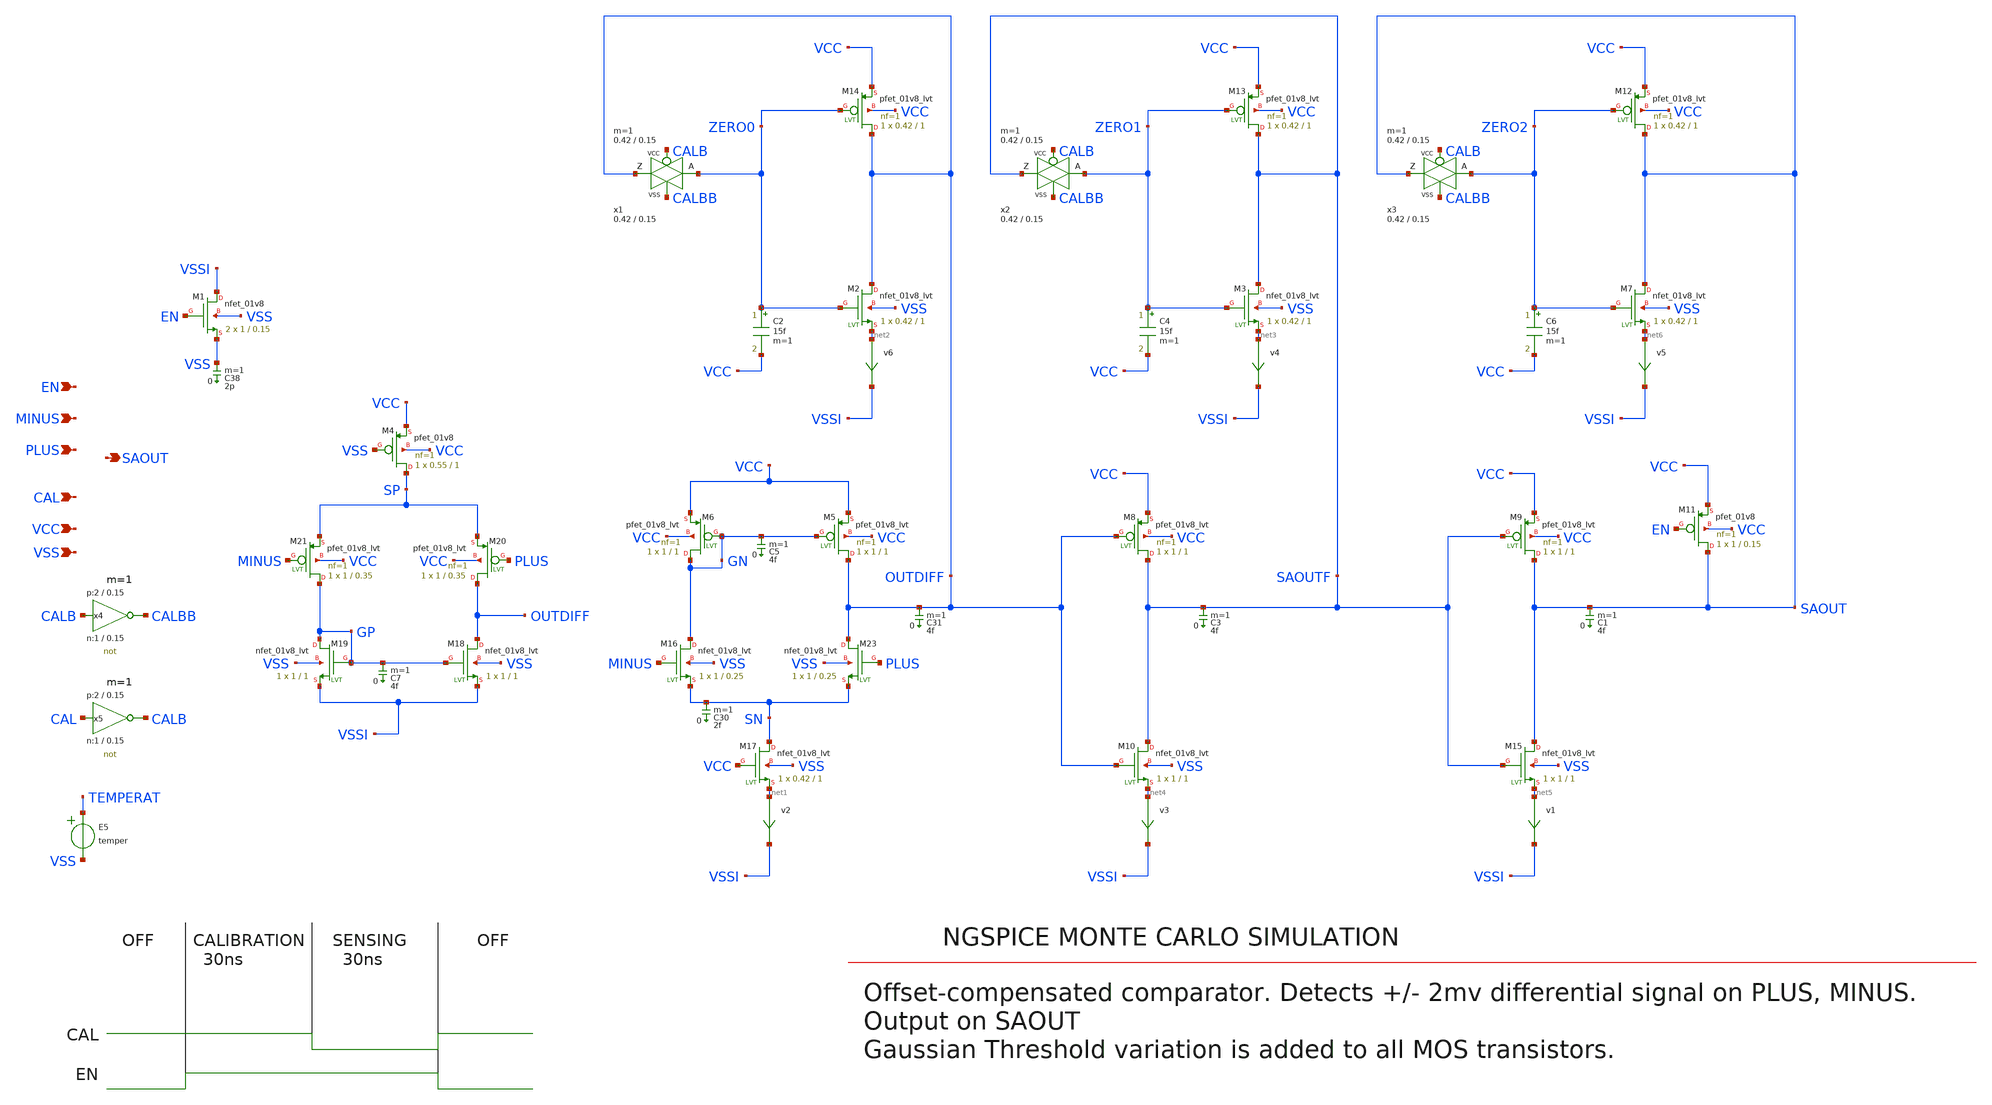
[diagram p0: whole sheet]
** sch_path: sky130_tests/test_comparator.sch
* Copyright 2020 Stefan Frederik Schippers
* Licensed under the Apache License, Version 2.0 (the "License");
* you may not use this file except in compliance with the License.
* You may obtain a copy of the License at
* https://www.apache.org/licenses/LICENSE-2.0
* Unless required by applicable law or agreed to in writing, software
* distributed under the License is distributed on an "AS IS" BASIS,
* WITHOUT WARRANTIES OR CONDITIONS OF ANY KIND, either express or implied.
* See the License for the specific language governing permissions and
* limitations under the License.
* sky130_tests/not.sch:
* Copyright 2021 Stefan Frederik Schippers
**.subckt test_comparator CAL PLUS MINUS EN VSS VCC SAOUT
*.ipin CAL
*.ipin PLUS
*.ipin MINUS
*.ipin EN
*.ipin VSS
*.ipin VCC
*.opin SAOUT
E5 TEMPERAT VSS VOL=' temper '
C38 VSS 0 2p m=1
C3 SAOUTF 0 4f m=1
C5 GN 0 4f m=1
C30 SN 0 2f m=1
C31 OUTDIFF 0 4f m=1
v2 net1 VSSI 0
.save i(v2)
v3 net4 VSSI 0
.save i(v3)
v4 net3 VSSI 0
.save i(v4)
v6 net2 VSSI 0
.save i(v6)
C1 SAOUT 0 4f m=1
v1 net5 VSSI 0
.save i(v1)
v5 net6 VSSI 0
.save i(v5)
C7 GP 0 4f m=1
x4 CALBB CALB VCC VSS not W_N=1 L_N=0.15 W_P=2 L_P=0.15 m=1
x5 CALB CAL VCC VSS not W_N=1 L_N=0.15 W_P=2 L_P=0.15 m=1
XM4 SP VSS VCC VCC sky130_fd_pr__pfet_01v8 L=1 W=0.55 nf=1 ad='W * 0.29' as='W * 0.29' pd='W + 2 * 0.29'
+ ps='W + 2 * 0.29' nrd=0 nrs=0 sa=0 sb=0 sd=0 mult=1 m=1
XM5 OUTDIFF GN VCC VCC sky130_fd_pr__pfet_01v8_lvt L=1 W=1 nf=1 ad='W * 0.29' as='W * 0.29' pd='W + 2 * 0.29'
+ ps='W + 2 * 0.29' nrd=0 nrs=0 sa=0 sb=0 sd=0 mult=1 m=1
XM6 GN GN VCC VCC sky130_fd_pr__pfet_01v8_lvt L=1 W=1 nf=1 ad='W * 0.29' as='W * 0.29' pd='W + 2 * 0.29'
+ ps='W + 2 * 0.29' nrd=0 nrs=0 sa=0 sb=0 sd=0 mult=1 m=1
XM8 SAOUTF OUTDIFF VCC VCC sky130_fd_pr__pfet_01v8_lvt L=1 W=1 nf=1 ad='W * 0.29' as='W * 0.29' pd='W + 2 * 0.29'
+ ps='W + 2 * 0.29' nrd=0 nrs=0 sa=0 sb=0 sd=0 mult=1 m=1
XM9 SAOUT SAOUTF VCC VCC sky130_fd_pr__pfet_01v8_lvt L=1 W=1 nf=1 ad='W * 0.29' as='W * 0.29' pd='W + 2 * 0.29'
+ ps='W + 2 * 0.29' nrd=0 nrs=0 sa=0 sb=0 sd=0 mult=1 m=1
XM11 SAOUT EN VCC VCC sky130_fd_pr__pfet_01v8 L=0.15 W=1 nf=1 ad='W * 0.29' as='W * 0.29' pd='W + 2 * 0.29'
+ ps='W + 2 * 0.29' nrd=0 nrs=0 sa=0 sb=0 sd=0 mult=1 m=1
XM12 SAOUT ZERO2 VCC VCC sky130_fd_pr__pfet_01v8_lvt L=1 W=0.42 nf=1 ad='W * 0.29' as='W * 0.29' pd='W + 2 * 0.29'
+ ps='W + 2 * 0.29' nrd=0 nrs=0 sa=0 sb=0 sd=0 mult=1 m=1
XM13 SAOUTF ZERO1 VCC VCC sky130_fd_pr__pfet_01v8_lvt L=1 W=0.42 nf=1 ad='W * 0.29' as='W * 0.29' pd='W + 2 * 0.29'
+ ps='W + 2 * 0.29' nrd=0 nrs=0 sa=0 sb=0 sd=0 mult=1 m=1
XM14 OUTDIFF ZERO0 VCC VCC sky130_fd_pr__pfet_01v8_lvt L=1 W=0.42 nf=1 ad='W * 0.29' as='W * 0.29' pd='W + 2 * 0.29'
+ ps='W + 2 * 0.29' nrd=0 nrs=0 sa=0 sb=0 sd=0 mult=1 m=1
XM1 VSSI EN VSS VSS sky130_fd_pr__nfet_01v8 W=1 L=0.15 ad='W * 0.29' pd='W + 2 * 0.29' as='W * 0.29'
+ ps='W + 2 * 0.29' nrd=0 nrs=0 sa=0 sb=0 sd=0 nf=1 mult=2 m=2
XM2 OUTDIFF ZERO0 net2 VSS sky130_fd_pr__nfet_01v8_lvt W=0.42 L=1 ad='W * 0.29' pd='W + 2 * 0.29' as='W * 0.29'
+ ps='W + 2 * 0.29' nrd=0 nrs=0 sa=0 sb=0 sd=0 nf=1 mult=1 m=1
XM3 SAOUTF ZERO1 net3 VSS sky130_fd_pr__nfet_01v8_lvt W=0.42 L=1 ad='W * 0.29' pd='W + 2 * 0.29' as='W * 0.29'
+ ps='W + 2 * 0.29' nrd=0 nrs=0 sa=0 sb=0 sd=0 nf=1 mult=1 m=1
XM7 SAOUT ZERO2 net6 VSS sky130_fd_pr__nfet_01v8_lvt W=0.42 L=1 ad='W * 0.29' pd='W + 2 * 0.29' as='W * 0.29'
+ ps='W + 2 * 0.29' nrd=0 nrs=0 sa=0 sb=0 sd=0 nf=1 mult=1 m=1
XM15 SAOUT SAOUTF net5 VSS sky130_fd_pr__nfet_01v8_lvt W=1 L=1 ad='W * 0.29' pd='W + 2 * 0.29' as='W * 0.29'
+ ps='W + 2 * 0.29' nrd=0 nrs=0 sa=0 sb=0 sd=0 nf=1 mult=1 m=1
XM10 SAOUTF OUTDIFF net4 VSS sky130_fd_pr__nfet_01v8_lvt W=1 L=1 ad='W * 0.29' pd='W + 2 * 0.29' as='W * 0.29'
+ ps='W + 2 * 0.29' nrd=0 nrs=0 sa=0 sb=0 sd=0 nf=1 mult=1 m=1
XM17 SN VCC net1 VSS sky130_fd_pr__nfet_01v8_lvt W=0.42 L=1 ad='W * 0.29' pd='W + 2 * 0.29' as='W * 0.29'
+ ps='W + 2 * 0.29' nrd=0 nrs=0 sa=0 sb=0 sd=0 nf=1 mult=1 m=1
XM18 OUTDIFF GP VSSI VSS sky130_fd_pr__nfet_01v8_lvt W=1 L=1 ad='W * 0.29' pd='W + 2 * 0.29' as='W * 0.29'
+ ps='W + 2 * 0.29' nrd=0 nrs=0 sa=0 sb=0 sd=0 nf=1 mult=1 m=1
XM19 GP GP VSSI VSS sky130_fd_pr__nfet_01v8_lvt W=1 L=1 ad='W * 0.29' pd='W + 2 * 0.29' as='W * 0.29'
+ ps='W + 2 * 0.29' nrd=0 nrs=0 sa=0 sb=0 sd=0 nf=1 mult=1 m=1
XM20 OUTDIFF PLUS SP VCC sky130_fd_pr__pfet_01v8_lvt L=0.35 W=1 nf=1 ad='W * 0.29' as='W * 0.29' pd='W + 2 * 0.29'
+ ps='W + 2 * 0.29' nrd=0 nrs=0 sa=0 sb=0 sd=0 mult=1 m=1
XM21 GP MINUS SP VCC sky130_fd_pr__pfet_01v8_lvt L=0.35 W=1 nf=1 ad='W * 0.29' as='W * 0.29' pd='W + 2 * 0.29'
+ ps='W + 2 * 0.29' nrd=0 nrs=0 sa=0 sb=0 sd=0 mult=1 m=1
XM23 OUTDIFF PLUS SN VSS sky130_fd_pr__nfet_01v8_lvt W=1 L=0.25 ad='W * 0.29' pd='W + 2 * 0.29' as='W * 0.29'
+ ps='W + 2 * 0.29' nrd=0 nrs=0 sa=0 sb=0 sd=0 nf=1 mult=1 m=1
XM16 GN MINUS SN VSS sky130_fd_pr__nfet_01v8_lvt W=1 L=0.25 ad='W * 0.29' pd='W + 2 * 0.29' as='W * 0.29'
+ ps='W + 2 * 0.29' nrd=0 nrs=0 sa=0 sb=0 sd=0 nf=1 mult=1 m=1
x1 OUTDIFF ZERO0 CALB CALBB VCC VSS passgate_nlvt W_N=0.42 L_N=0.15 W_P=0.42 L_P=0.15 ad=0.12
+ as=0.12 pd=0.9 ps=1
x2 SAOUTF ZERO1 CALB CALBB VCC VSS passgate_nlvt W_N=0.42 L_N=0.15 W_P=0.42 L_P=0.15 ad=0.12 as=0.12
+ pd=0.9 ps=1
x3 SAOUT ZERO2 CALB CALBB VCC VSS passgate_nlvt W_N=0.42 L_N=0.15 W_P=0.42 L_P=0.15 ad=0.12 as=0.12
+ pd=0.9 ps=1
C2 ZERO0 VCC 15f m=1
C4 ZERO1 VCC 15f m=1
C6 ZERO2 VCC 15f m=1
**.ends

* expanding   symbol:  sky130_tests/not.sym # of pins=2
** sym_path: sky130_tests/not.sym
** sch_path: sky130_tests/not.sch
.subckt not y a VCCPIN VSSPIN     W_N=1 L_N=0.15 W_P=2 L_P=0.15
*.opin y
*.ipin a
XM1 DN a VSSPIN VSSPIN sky130_fd_pr__nfet_01v8 W=W_N L=L_N ad='W * 0.29' pd='2 * (W + 0.29)' as='W * 0.29'
+ ps='2 * (W + 0.29)' nrd='0.29 / W' nrs='0.29 / W' sa=0 sb=0 sd=0 nf=1 mult=1 m=1
XM2 DP a VCCPIN VCCPIN sky130_fd_pr__pfet_01v8 L=L_P W=W_P nf=1 ad='int((nf+1)/2) * W/nf * 0.29' as='int((nf+2)/2) * W/nf * 0.29'
+ pd='2*int((nf+1)/2) * (W/nf + 0.29)' ps='2*int((nf+2)/2) * (W/nf + 0.29)' nrd='0.29 / W' nrs='0.29 / W'
+ sa=0 sb=0 sd=0 mult=1 m=1
Vmeas DP y 0
.save i(vmeas)
Vmeas1 y DN 0
.save i(vmeas1)
.save v(dp)
.save v(dn)
.ends


* expanding   symbol:  sky130_tests/passgate_nlvt.sym # of pins=4
** sym_path: sky130_tests/passgate_nlvt.sym
** sch_path: sky130_tests/passgate_nlvt.sch
.subckt passgate_nlvt Z A GP GN VCCBPIN VSSBPIN  W_N=1 L_N=0.2 W_P=1 L_P=0.2   ad=0 as=0 pd=0 ps=0
*.iopin A
*.iopin Z
*.ipin GP
*.ipin GN
XM1 net1 GN net2 VSS sky130_fd_pr__nfet_01v8_lvt W=W_N L=L_N ad=ad pd=pd as=as ps=ps nrd=0 nrs=0
+ sa=0 sb=0 sd=0 nf=1 mult=1 m=1
XM2 A GP Z VCC sky130_fd_pr__pfet_01v8 W=W_P L=L_P ad=ad pd=pd as=as ps=ps nrd=0 nrs=0 sa=0 sb=0
+ sd=0 nf=1 mult=1
.ends

**** begin user architecture code

* .option SCALE=1e-6
.option method=gear seed=12
.param VCC=1.8
.param VCCGAUSS=agauss(1.8, 0.05, 1)
.param VCC=VCCGAUSS
.param VDL='VCC/2+0.2'
.param ABSVAR=0.02
.temp 25

** to generate following file:
** copy .../xschem_sky130/sky130_tests/stimuli.test_comparator to simulation directory
** then do 'Simulation->Utile Stimuli Editor (GUI)' and press 'Translate'
.include "stimuli_test_comparator.cir"

*.lib ~/sky130_fd_pr/models/sky130.lib.spice tt

* temporary fix: some model equations use temp instead of the true
* ngspice temperature variable, 'temper'
.param temp=27

** variation marameters:
.param sky130_fd_pr__nfet_01v8_lvt__vth0_slope_spectre='agauss(0, ABSVAR, 3)/sky130_fd_pr__nfet_01v8_lvt__vth0_slope'
.param sky130_fd_pr__pfet_01v8_lvt__vth0_slope_spectre='agauss(0, ABSVAR, 3)/sky130_fd_pr__pfet_01v8_lvt__vth0_slope'

* .tran 0.1n 900n uic

.control
  let run=1

  dowhile run <= 10
    if run > 1
      reset
      set appendwrite
    end
    * save saout cal i(vvcc) en plus minus
    tran 0.1n 300n uic
    write test_comparator.raw
    let run = run + 1
  end
.endc



.include ~/sky130_fd_pr/cells/nfet_01v8/sky130_fd_pr__nfet_01v8__tt.corner.spice
.include ~/sky130_fd_pr/cells/nfet_01v8_lvt/sky130_fd_pr__nfet_01v8_lvt__tt.corner.spice
.include ~/sky130_fd_pr/cells/pfet_01v8/sky130_fd_pr__pfet_01v8__tt.corner.spice
.include ~/sky130_fd_pr/cells/nfet_03v3_nvt/sky130_fd_pr__nfet_03v3_nvt__tt.corner.spice
.include ~/sky130_fd_pr/cells/nfet_05v0_nvt/sky130_fd_pr__nfet_05v0_nvt__tt.corner.spice
.include ~/sky130_fd_pr/cells/esd_nfet_01v8/sky130_fd_pr__esd_nfet_01v8__tt.corner.spice
.include ~/sky130_fd_pr/cells/pfet_01v8_lvt/sky130_fd_pr__pfet_01v8_lvt__tt.corner.spice
.include ~/sky130_fd_pr/cells/pfet_01v8_hvt/sky130_fd_pr__pfet_01v8_hvt__tt.corner.spice
.include ~/sky130_fd_pr/cells/esd_pfet_g5v0d10v5/sky130_fd_pr__esd_pfet_g5v0d10v5__tt.corner.spice
.include ~/sky130_fd_pr/cells/pfet_g5v0d10v5/sky130_fd_pr__pfet_g5v0d10v5__tt.corner.spice
.include ~/sky130_fd_pr/cells/pfet_g5v0d16v0/sky130_fd_pr__pfet_g5v0d16v0__tt.corner.spice
.include ~/sky130_fd_pr/cells/nfet_g5v0d10v5/sky130_fd_pr__nfet_g5v0d10v5__tt.corner.spice
.include ~/sky130_fd_pr/cells/nfet_g5v0d16v0/sky130_fd_pr__nfet_g5v0d16v0__tt_discrete.corner.spice
.include ~/sky130_fd_pr/cells/esd_nfet_g5v0d10v5/sky130_fd_pr__esd_nfet_g5v0d10v5__tt.corner.spice
.include ~/sky130_fd_pr/models/corners/tt/nonfet.spice
* Mismatch parameters
.include ~/sky130_fd_pr/cells/nfet_01v8/sky130_fd_pr__nfet_01v8__mismatch.corner.spice
.include ~/sky130_fd_pr/cells/pfet_01v8/sky130_fd_pr__pfet_01v8__mismatch.corner.spice
.include ~/sky130_fd_pr/cells/nfet_01v8_lvt/sky130_fd_pr__nfet_01v8_lvt__mismatch.corner.spice
.include ~/sky130_fd_pr/cells/pfet_01v8_lvt/sky130_fd_pr__pfet_01v8_lvt__mismatch.corner.spice
.include ~/sky130_fd_pr/cells/pfet_01v8_hvt/sky130_fd_pr__pfet_01v8_hvt__mismatch.corner.spice
.include ~/sky130_fd_pr/cells/nfet_g5v0d10v5/sky130_fd_pr__nfet_g5v0d10v5__mismatch.corner.spice
.include ~/sky130_fd_pr/cells/pfet_g5v0d10v5/sky130_fd_pr__pfet_g5v0d10v5__mismatch.corner.spice
.include ~/sky130_fd_pr/cells/nfet_05v0_nvt/sky130_fd_pr__nfet_05v0_nvt__mismatch.corner.spice
.include ~/sky130_fd_pr/cells/nfet_03v3_nvt/sky130_fd_pr__nfet_03v3_nvt__mismatch.corner.spice
* Resistor/Capacitor
.include ~/sky130_fd_pr/models/r+c/res_typical__cap_typical.spice
.include ~/sky130_fd_pr/models/r+c/res_typical__cap_typical__lin.spice
* Special cells
.include ~/sky130_fd_pr/models/corners/tt/specialized_cells.spice
* All models
.include ~/sky130_fd_pr/models/all.spice
* Corner
.include ~/sky130_fd_pr/models/corners/tt/rf.spice


**** end user architecture code
.end
